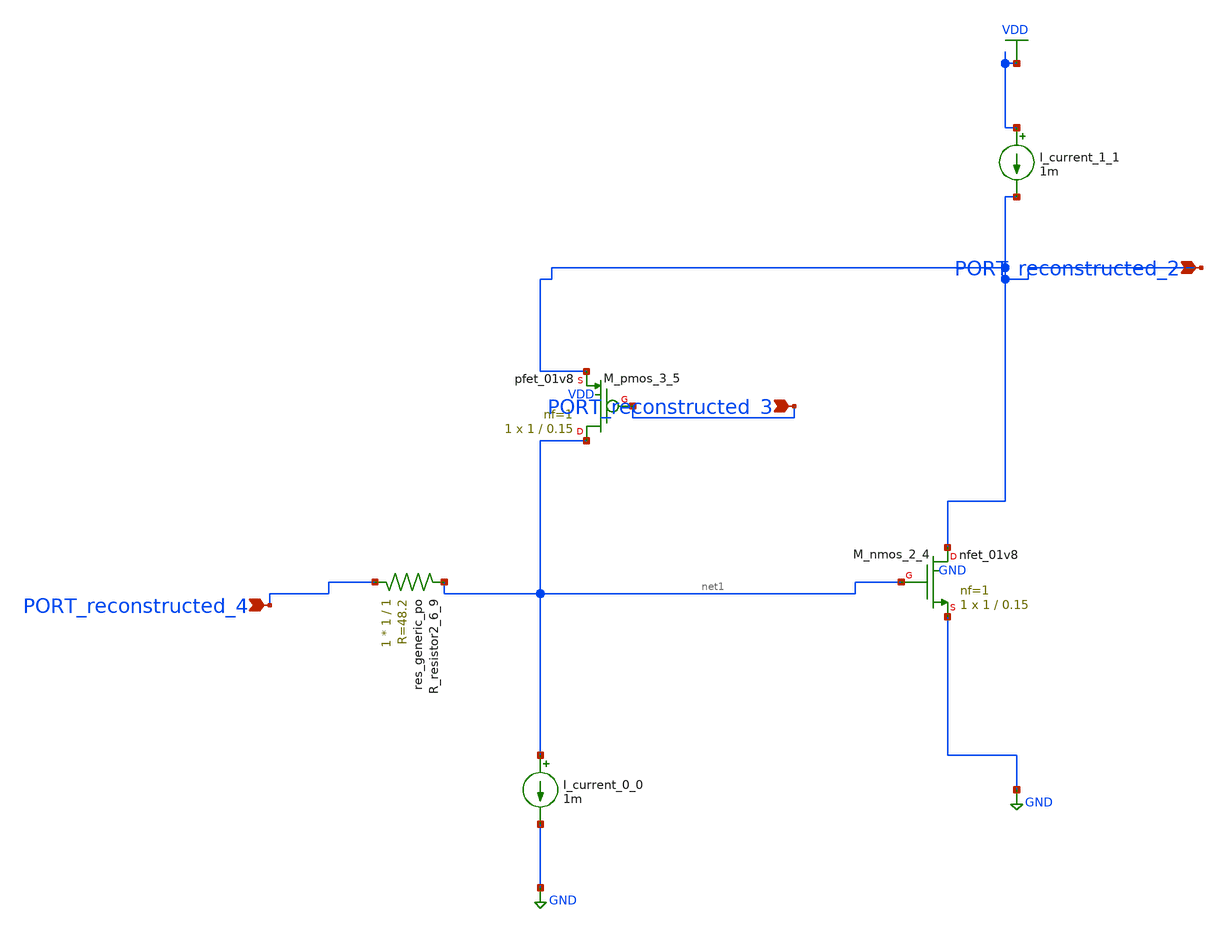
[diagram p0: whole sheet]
** sch_path: schematics/AMSNet/413.sch
**.subckt 413 PORT_reconstructed_3 PORT_reconstructed_2 PORT_reconstructed_4
*.ipin PORT_reconstructed_3
*.ipin PORT_reconstructed_2
*.ipin PORT_reconstructed_4
I_current_0_0 net1 GND 1m
I_current_1_1 VDD PORT_reconstructed_2 1m
XM_nmos_2_4 PORT_reconstructed_2 net1 GND GND sky130_fd_pr__nfet_01v8 L=0.15 W=1 nf=1 ad='int((1 + 1)/2) * 1 / 1 * 0.29'
+ as='int((1 + 2)/2) * 1 / 1 * 0.29' pd='2*int((1 + 1)/2) * (1 / 1 + 0.29)' ps='2*int((1 + 2)/2) * (1 / 1 + 0.29)'
+ nrd='0.29 / 1 ' nrs='0.29 / 1 ' sa=0 sb=0 sd=0 mult=1 m=1
XM_pmos_3_5 net1 PORT_reconstructed_3 PORT_reconstructed_2 VDD sky130_fd_pr__pfet_01v8 L=0.15 W=1 nf=1
+ ad='int((1 + 1)/2) * 1 / 1 * 0.29' as='int((1 + 2)/2) * 1 / 1 * 0.29' pd='2*int((1 + 1)/2) * (1 / 1 + 0.29)'
+ ps='2*int((1 + 2)/2) * (1 / 1 + 0.29)' nrd='0.29 / 1 ' nrs='0.29 / 1 ' sa=0 sb=0 sd=0 mult=1 m=1
XR_resistor2_6_9 PORT_reconstructed_4 net1 sky130_fd_pr__res_generic_po W=1 L=1 m=1
**.ends
.GLOBAL GND
.GLOBAL VDD
.end
